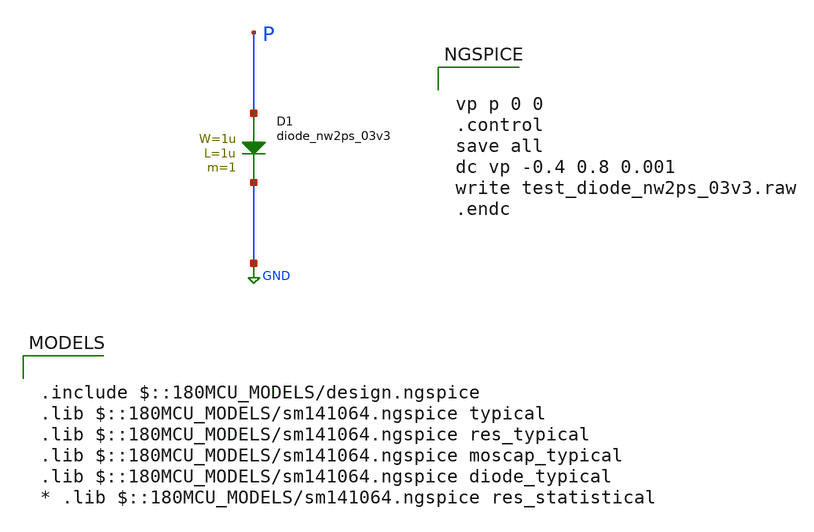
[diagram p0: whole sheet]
** sch_path: gf180mcuD/xschem_libs/gf180mcu_tests/test_diode_nw2ps_03v3/schematic/test_diode_nw2ps_03v3.sch
* Copyright 2022 GlobalFoundries PDK Authors
* Licensed under the Apache License, Version 2.0 (the "License");
* you may not use this file except in compliance with the License.
* You may obtain a copy of the License at
* https://www.apache.org/licenses/LICENSE-2.0
* Unless required by applicable law or agreed to in writing, software
* distributed under the License is distributed on an "AS IS" BASIS,
* WITHOUT WARRANTIES OR CONDITIONS OF ANY KIND, either express or implied.
* See the License for the specific language governing permissions and
* limitations under the License.
**.subckt test_diode_nw2ps_03v3
D1 P GND diode_nw2ps_03v3 area='1u * 1u ' pj='2*1u + 2*1u ' m=1
**** begin user architecture code

.include $::180MCU_MODELS/design.ngspice
.lib $::180MCU_MODELS/sm141064.ngspice typical
.lib $::180MCU_MODELS/sm141064.ngspice res_typical
.lib $::180MCU_MODELS/sm141064.ngspice moscap_typical
.lib $::180MCU_MODELS/sm141064.ngspice diode_typical
* .lib $::180MCU_MODELS/sm141064.ngspice res_statistical



vp p 0 0
.control
save all
dc vp -0.4 0.8 0.001
write test_diode_nw2ps_03v3.raw
.endc


**** end user architecture code
**.ends
.GLOBAL GND
.end
